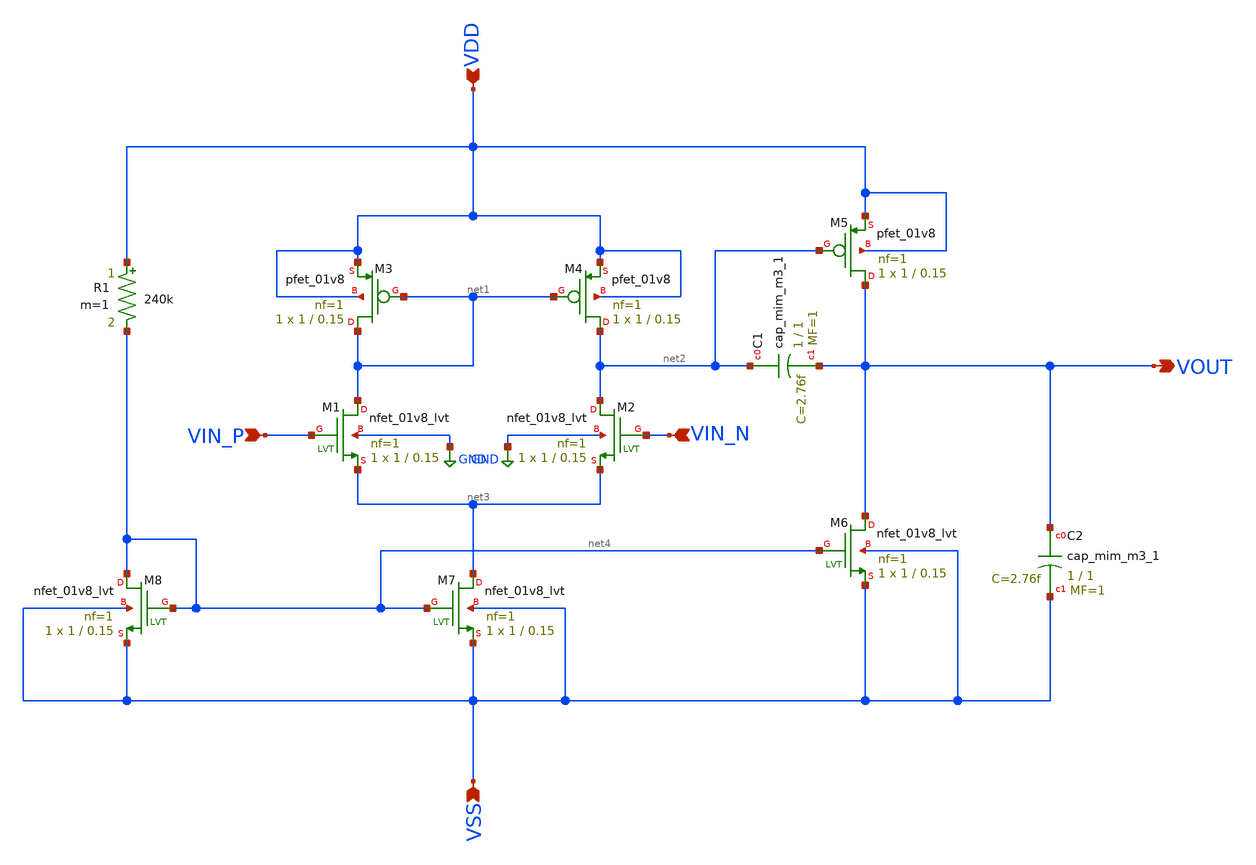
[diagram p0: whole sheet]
** sch_path: analog/schematics/opamp_single_stage.sch.sch
**.subckt opamp_single_stage.sch VDD VIN_P VIN_N VSS VOUT
*.ipin VDD
*.ipin VIN_P
*.ipin VIN_N
*.ipin VSS
*.opin VOUT
XM4 net2 net1 VDD VDD sky130_fd_pr__pfet_01v8 L=0.15 W=1 nf=1 ad='int((nf+1)/2) * W/nf * 0.29' as='int((nf+2)/2) * W/nf * 0.29'
+ pd='2*int((nf+1)/2) * (W/nf + 0.29)' ps='2*int((nf+2)/2) * (W/nf + 0.29)' nrd='0.29 / W' nrs='0.29 / W'
+ sa=0 sb=0 sd=0 mult=1 m=1
XM3 net1 net1 VDD VDD sky130_fd_pr__pfet_01v8 L=0.15 W=1 nf=1 ad='int((nf+1)/2) * W/nf * 0.29' as='int((nf+2)/2) * W/nf * 0.29'
+ pd='2*int((nf+1)/2) * (W/nf + 0.29)' ps='2*int((nf+2)/2) * (W/nf + 0.29)' nrd='0.29 / W' nrs='0.29 / W'
+ sa=0 sb=0 sd=0 mult=1 m=1
XM1 net1 VIN_P net3 GND sky130_fd_pr__nfet_01v8_lvt L=0.15 W=1 nf=1 ad='int((nf+1)/2) * W/nf * 0.29'
+ as='int((nf+2)/2) * W/nf * 0.29' pd='2*int((nf+1)/2) * (W/nf + 0.29)' ps='2*int((nf+2)/2) * (W/nf + 0.29)'
+ nrd='0.29 / W' nrs='0.29 / W' sa=0 sb=0 sd=0 mult=1 m=1
XM2 net2 VIN_N net3 GND sky130_fd_pr__nfet_01v8_lvt L=0.15 W=1 nf=1 ad='int((nf+1)/2) * W/nf * 0.29'
+ as='int((nf+2)/2) * W/nf * 0.29' pd='2*int((nf+1)/2) * (W/nf + 0.29)' ps='2*int((nf+2)/2) * (W/nf + 0.29)'
+ nrd='0.29 / W' nrs='0.29 / W' sa=0 sb=0 sd=0 mult=1 m=1
XM5 VOUT net2 VDD VDD sky130_fd_pr__pfet_01v8 L=0.15 W=1 nf=1 ad='int((nf+1)/2) * W/nf * 0.29' as='int((nf+2)/2) * W/nf * 0.29'
+ pd='2*int((nf+1)/2) * (W/nf + 0.29)' ps='2*int((nf+2)/2) * (W/nf + 0.29)' nrd='0.29 / W' nrs='0.29 / W'
+ sa=0 sb=0 sd=0 mult=1 m=1
XC1 net2 VOUT sky130_fd_pr__cap_mim_m3_1 W=1 L=1 MF=1 m=1
XM8 net4 net4 VSS VSS sky130_fd_pr__nfet_01v8_lvt L=0.15 W=1 nf=1 ad='int((nf+1)/2) * W/nf * 0.29' as='int((nf+2)/2) * W/nf * 0.29'
+ pd='2*int((nf+1)/2) * (W/nf + 0.29)' ps='2*int((nf+2)/2) * (W/nf + 0.29)' nrd='0.29 / W' nrs='0.29 / W'
+ sa=0 sb=0 sd=0 mult=1 m=1
XM7 net3 net4 VSS VSS sky130_fd_pr__nfet_01v8_lvt L=0.15 W=1 nf=1 ad='int((nf+1)/2) * W/nf * 0.29' as='int((nf+2)/2) * W/nf * 0.29'
+ pd='2*int((nf+1)/2) * (W/nf + 0.29)' ps='2*int((nf+2)/2) * (W/nf + 0.29)' nrd='0.29 / W' nrs='0.29 / W'
+ sa=0 sb=0 sd=0 mult=1 m=1
XM6 VOUT net4 VSS VSS sky130_fd_pr__nfet_01v8_lvt L=0.15 W=1 nf=1 ad='int((nf+1)/2) * W/nf * 0.29' as='int((nf+2)/2) * W/nf * 0.29'
+ pd='2*int((nf+1)/2) * (W/nf + 0.29)' ps='2*int((nf+2)/2) * (W/nf + 0.29)' nrd='0.29 / W' nrs='0.29 / W'
+ sa=0 sb=0 sd=0 mult=1 m=1
XC2 VOUT VSS sky130_fd_pr__cap_mim_m3_1 W=1 L=1 MF=1 m=1
R1 VDD net4 240k m=1
**.ends
.GLOBAL GND
.end
